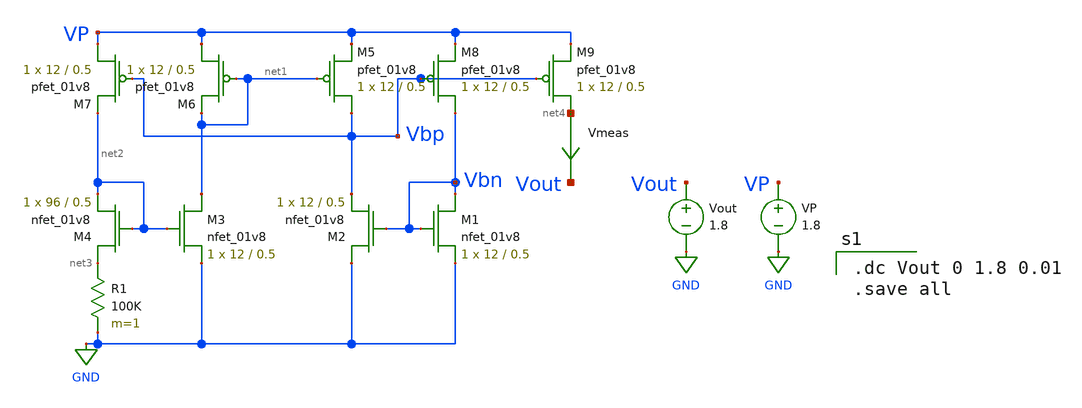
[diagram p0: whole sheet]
** sch_path: xschem/test_cur_gen.sch
**.subckt test_cur_gen
XM1 Vbn Vbn GND GND sky130_fd_pr__nfet_01v8 L=0.5 W=12 nf=1 ad='int((nf+1)/2) * W/nf * 0.29' as='int((nf+2)/2) * W/nf * 0.29'
+ pd='2*int((nf+1)/2) * (W/nf + 0.29)' ps='2*int((nf+2)/2) * (W/nf + 0.29)' nrd='0.29 / W' nrs='0.29 / W'
+ sa=0 sb=0 sd=0 mult=1 m=1
XM2 GND Vbn Vbp GND sky130_fd_pr__nfet_01v8 L=0.5 W=12 nf=1 ad='int((nf+1)/2) * W/nf * 0.29' as='int((nf+2)/2) * W/nf * 0.29'
+ pd='2*int((nf+1)/2) * (W/nf + 0.29)' ps='2*int((nf+2)/2) * (W/nf + 0.29)' nrd='0.29 / W' nrs='0.29 / W'
+ sa=0 sb=0 sd=0 mult=1 m=1
XM3 net1 net2 GND GND sky130_fd_pr__nfet_01v8 L=0.5 W=12 nf=1 ad='int((nf+1)/2) * W/nf * 0.29' as='int((nf+2)/2) * W/nf * 0.29'
+ pd='2*int((nf+1)/2) * (W/nf + 0.29)' ps='2*int((nf+2)/2) * (W/nf + 0.29)' nrd='0.29 / W' nrs='0.29 / W'
+ sa=0 sb=0 sd=0 mult=1 m=1
XM4 net3 net2 net2 GND sky130_fd_pr__nfet_01v8 L=0.5 W=96 nf=1 ad='int((nf+1)/2) * W/nf * 0.29' as='int((nf+2)/2) * W/nf * 0.29'
+ pd='2*int((nf+1)/2) * (W/nf + 0.29)' ps='2*int((nf+2)/2) * (W/nf + 0.29)' nrd='0.29 / W' nrs='0.29 / W'
+ sa=0 sb=0 sd=0 mult=1 m=1
XM5 Vbp net1 VP VDD sky130_fd_pr__pfet_01v8 L=0.5 W=12 nf=1 ad='int((nf+1)/2) * W/nf * 0.29' as='int((nf+2)/2) * W/nf * 0.29'
+ pd='2*int((nf+1)/2) * (W/nf + 0.29)' ps='2*int((nf+2)/2) * (W/nf + 0.29)' nrd='0.29 / W' nrs='0.29 / W'
+ sa=0 sb=0 sd=0 mult=1 m=1
XM6 VP net1 net1 VDD sky130_fd_pr__pfet_01v8 L=0.5 W=12 nf=1 ad='int((nf+1)/2) * W/nf * 0.29' as='int((nf+2)/2) * W/nf * 0.29'
+ pd='2*int((nf+1)/2) * (W/nf + 0.29)' ps='2*int((nf+2)/2) * (W/nf + 0.29)' nrd='0.29 / W' nrs='0.29 / W'
+ sa=0 sb=0 sd=0 mult=1 m=1
XM7 VP Vbp net2 VDD sky130_fd_pr__pfet_01v8 L=0.5 W=12 nf=1 ad='int((nf+1)/2) * W/nf * 0.29' as='int((nf+2)/2) * W/nf * 0.29'
+ pd='2*int((nf+1)/2) * (W/nf + 0.29)' ps='2*int((nf+2)/2) * (W/nf + 0.29)' nrd='0.29 / W' nrs='0.29 / W'
+ sa=0 sb=0 sd=0 mult=1 m=1
XM8 Vbn Vbp VP VDD sky130_fd_pr__pfet_01v8 L=0.5 W=12 nf=1 ad='int((nf+1)/2) * W/nf * 0.29' as='int((nf+2)/2) * W/nf * 0.29'
+ pd='2*int((nf+1)/2) * (W/nf + 0.29)' ps='2*int((nf+2)/2) * (W/nf + 0.29)' nrd='0.29 / W' nrs='0.29 / W'
+ sa=0 sb=0 sd=0 mult=1 m=1
R1 net3 GND 100K m=1
VP VP GND 1.8
XM9 net4 Vbp VP VDD sky130_fd_pr__pfet_01v8 L=0.5 W=12 nf=1 ad='int((nf+1)/2) * W/nf * 0.29' as='int((nf+2)/2) * W/nf * 0.29'
+ pd='2*int((nf+1)/2) * (W/nf + 0.29)' ps='2*int((nf+2)/2) * (W/nf + 0.29)' nrd='0.29 / W' nrs='0.29 / W'
+ sa=0 sb=0 sd=0 mult=1 m=1
Vmeas net4 Vout 0
.save i(vmeas)
Vout Vout GND 1.8
**** begin user architecture code

.option wnflag=1
.param MC_SWITCH=0.0
.lib ~/skywater/skywater-pdk/libraries/sky130_fd_pr_ngspice/latest/models/sky130.lib.spice tt


.dc Vout 0 1.8 0.01
.save all

**** end user architecture code
**.ends
.GLOBAL GND
.end
